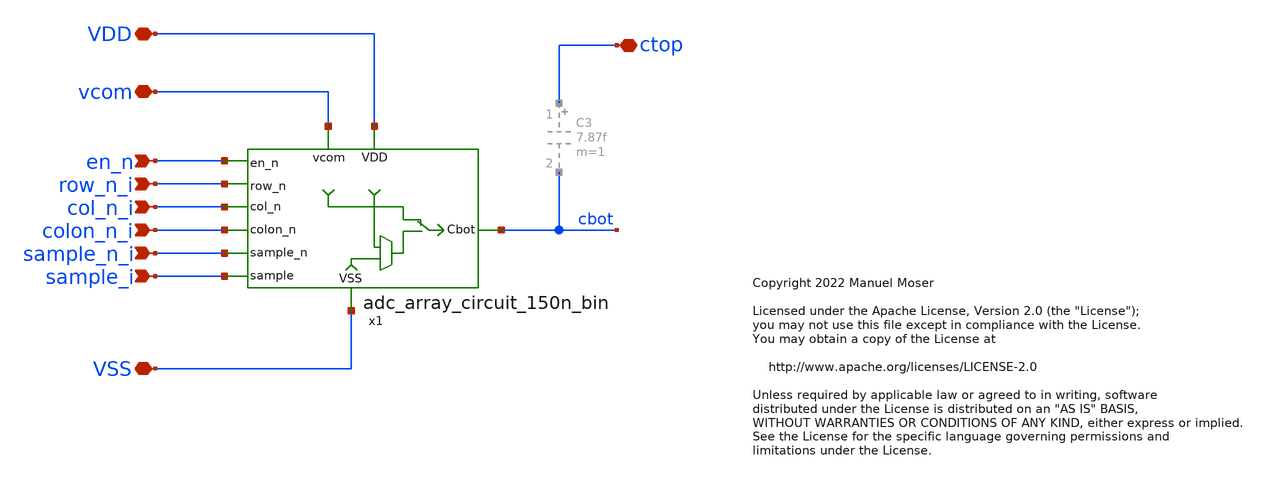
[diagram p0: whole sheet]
** sch_path: xschem/adc_array_cap_150n/adc_array_cap_bin.sch
* Copyright 2022 Manuel Moser
* Licensed under the Apache License, Version 2.0 (the "License");
**.subckt adc_array_cap_bin vcom VDD ctop VSS en_n row_n_i col_n_i colon_n_i sample_n_i sample_i
*.iopin vcom
*.iopin VDD
*.iopin ctop
*.iopin VSS
*.ipin en_n
*.ipin row_n_i
*.ipin col_n_i
*.ipin colon_n_i
*.ipin sample_n_i
*.ipin sample_i
x1 VDD row_n_i cbot col_n_i colon_n_i sample_n_i vcom sample_i VSS en_n adc_array_circuit_150n_bin
**.ends

* expanding   symbol:
*+  /foss/designs/SKY130_SAR-ADC/xschem/adc_array_circuit_150n/adc_array_circuit_150n_bin.sym # of pins=10
** sym_path: xschem/adc_array_circuit_150n/adc_array_circuit_150n_bin.sym
** sch_path: xschem/adc_array_circuit_150n/adc_array_circuit_150n_bin.sch
.subckt adc_array_circuit_150n_bin VDD row_n Cbot col_n colon_n sample_n vcom sample VSS en_n
*.ipin sample_n
*.ipin sample
*.iopin vcom
*.ipin row_n
*.ipin col_n
*.ipin colon_n
*.iopin VDD
*.iopin VSS
*.iopin Cbot
*.ipin en_n
XM1 vcom sample Cbot VSS sky130_fd_pr__nfet_01v8 L=0.15 W=0.42 nf=1 ad='int((nf+1)/2) * W/nf * 0.29'
+ as='int((nf+2)/2) * W/nf * 0.29' pd='2*int((nf+1)/2) * (W/nf + 0.29)' ps='2*int((nf+2)/2) * (W/nf + 0.29)'
+ nrd='0.29 / W' nrs='0.29 / W' sa=0 sb=0 sd=0 mult=1 m=1
XM3 vcom sample_n Cbot VDD sky130_fd_pr__pfet_01v8 L=0.15 W=0.8 nf=1 ad='int((nf+1)/2) * W/nf * 0.29'
+ as='int((nf+2)/2) * W/nf * 0.29' pd='2*int((nf+1)/2) * (W/nf + 0.29)' ps='2*int((nf+2)/2) * (W/nf + 0.29)'
+ nrd='0.29 / W' nrs='0.29 / W' sa=0 sb=0 sd=0 mult=1 m=1
XM2 vdrv sample_n Cbot VSS sky130_fd_pr__nfet_01v8 L=0.15 W=0.42 nf=1 ad='int((nf+1)/2) * W/nf * 0.29'
+ as='int((nf+2)/2) * W/nf * 0.29' pd='2*int((nf+1)/2) * (W/nf + 0.29)' ps='2*int((nf+2)/2) * (W/nf + 0.29)'
+ nrd='0.29 / W' nrs='0.29 / W' sa=0 sb=0 sd=0 mult=1 m=1
XM4 vdrv sample Cbot VDD sky130_fd_pr__pfet_01v8 L=0.15 W=0.8 nf=1 ad='int((nf+1)/2) * W/nf * 0.29' as='int((nf+2)/2) * W/nf * 0.29'
+ pd='2*int((nf+1)/2) * (W/nf + 0.29)' ps='2*int((nf+2)/2) * (W/nf + 0.29)' nrd='0.29 / W' nrs='0.29 / W'
+ sa=0 sb=0 sd=0 mult=1 m=1
XM5 vint1 en_n vdrv VDD sky130_fd_pr__pfet_01v8 L=0.15 W=0.8 nf=1 ad='int((nf+1)/2) * W/nf * 0.29' as='int((nf+2)/2) * W/nf * 0.29'
+ pd='2*int((nf+1)/2) * (W/nf + 0.29)' ps='2*int((nf+2)/2) * (W/nf + 0.29)' nrd='0.29 / W' nrs='0.29 / W'
+ sa=0 sb=0 sd=0 mult=1 m=1
XM6 VDD en_n vint1 VDD sky130_fd_pr__pfet_01v8 L=0.15 W=0.8 nf=1 ad='int((nf+1)/2) * W/nf * 0.29' as='int((nf+2)/2) * W/nf * 0.29'
+ pd='2*int((nf+1)/2) * (W/nf + 0.29)' ps='2*int((nf+2)/2) * (W/nf + 0.29)' nrd='0.29 / W' nrs='0.29 / W'
+ sa=0 sb=0 sd=0 mult=1 m=1
XM7 VDD en_n vdrv VDD sky130_fd_pr__pfet_01v8 L=0.15 W=0.8 nf=1 ad='int((nf+1)/2) * W/nf * 0.29' as='int((nf+2)/2) * W/nf * 0.29'
+ pd='2*int((nf+1)/2) * (W/nf + 0.29)' ps='2*int((nf+2)/2) * (W/nf + 0.29)' nrd='0.29 / W' nrs='0.29 / W'
+ sa=0 sb=0 sd=0 mult=1 m=1
XM8 vint2 en_n vdrv VSS sky130_fd_pr__nfet_01v8 L=0.15 W=0.42 nf=1 ad='int((nf+1)/2) * W/nf * 0.29' as='int((nf+2)/2) * W/nf * 0.29'
+ pd='2*int((nf+1)/2) * (W/nf + 0.29)' ps='2*int((nf+2)/2) * (W/nf + 0.29)' nrd='0.29 / W' nrs='0.29 / W'
+ sa=0 sb=0 sd=0 mult=1 m=1
XM9 VSS en_n vint2 VSS sky130_fd_pr__nfet_01v8 L=0.15 W=0.42 nf=1 ad='int((nf+1)/2) * W/nf * 0.29' as='int((nf+2)/2) * W/nf * 0.29'
+ pd='2*int((nf+1)/2) * (W/nf + 0.29)' ps='2*int((nf+2)/2) * (W/nf + 0.29)' nrd='0.29 / W' nrs='0.29 / W'
+ sa=0 sb=0 sd=0 mult=1 m=1
XM10 VSS en_n vint2 VSS sky130_fd_pr__nfet_01v8 L=0.15 W=0.42 nf=1 ad='int((nf+1)/2) * W/nf * 0.29' as='int((nf+2)/2) * W/nf * 0.29'
+ pd='2*int((nf+1)/2) * (W/nf + 0.29)' ps='2*int((nf+2)/2) * (W/nf + 0.29)' nrd='0.29 / W' nrs='0.29 / W'
+ sa=0 sb=0 sd=0 mult=1 m=1
* noconn row_n
* noconn col_n
* noconn colon_n
.ends

.end
